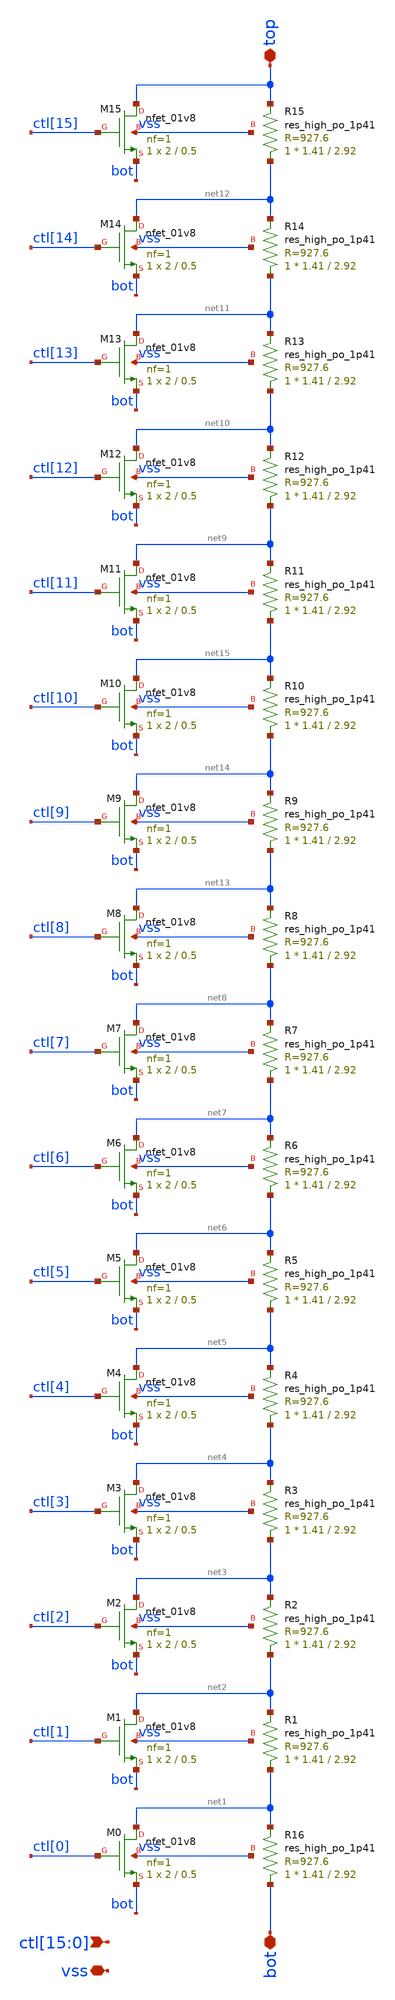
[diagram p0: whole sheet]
** sch_path: xschem/bandgap/bg_trim.sch
**.subckt bg_trim vss
*+ ctl[15],ctl[14],ctl[13],ctl[12],ctl[11],ctl[10],ctl[9],ctl[8],ctl[7],ctl[6],ctl[5],ctl[4],ctl[3],ctl[2],ctl[1],ctl[0] bot top
*.iopin vss
*.ipin
*+ ctl[15],ctl[14],ctl[13],ctl[12],ctl[11],ctl[10],ctl[9],ctl[8],ctl[7],ctl[6],ctl[5],ctl[4],ctl[3],ctl[2],ctl[1],ctl[0]
*.iopin bot
*.iopin top
XM0 net1 ctl[0] bot vss sky130_fd_pr__nfet_01v8 L=0.5 W=2 nf=1 ad='int((nf+1)/2) * W/nf * 0.29' as='int((nf+2)/2) * W/nf * 0.29'
+ pd='2*int((nf+1)/2) * (W/nf + 0.29)' ps='2*int((nf+2)/2) * (W/nf + 0.29)' nrd='0.29 / W' nrs='0.29 / W'
+ sa=0 sb=0 sd=0 mult=1 m=1
XM1 net2 ctl[1] bot vss sky130_fd_pr__nfet_01v8 L=0.5 W=2 nf=1 ad='int((nf+1)/2) * W/nf * 0.29' as='int((nf+2)/2) * W/nf * 0.29'
+ pd='2*int((nf+1)/2) * (W/nf + 0.29)' ps='2*int((nf+2)/2) * (W/nf + 0.29)' nrd='0.29 / W' nrs='0.29 / W'
+ sa=0 sb=0 sd=0 mult=1 m=1
XM2 net3 ctl[2] bot vss sky130_fd_pr__nfet_01v8 L=0.5 W=2 nf=1 ad='int((nf+1)/2) * W/nf * 0.29' as='int((nf+2)/2) * W/nf * 0.29'
+ pd='2*int((nf+1)/2) * (W/nf + 0.29)' ps='2*int((nf+2)/2) * (W/nf + 0.29)' nrd='0.29 / W' nrs='0.29 / W'
+ sa=0 sb=0 sd=0 mult=1 m=1
XM3 net4 ctl[3] bot vss sky130_fd_pr__nfet_01v8 L=0.5 W=2 nf=1 ad='int((nf+1)/2) * W/nf * 0.29' as='int((nf+2)/2) * W/nf * 0.29'
+ pd='2*int((nf+1)/2) * (W/nf + 0.29)' ps='2*int((nf+2)/2) * (W/nf + 0.29)' nrd='0.29 / W' nrs='0.29 / W'
+ sa=0 sb=0 sd=0 mult=1 m=1
XM4 net5 ctl[4] bot vss sky130_fd_pr__nfet_01v8 L=0.5 W=2 nf=1 ad='int((nf+1)/2) * W/nf * 0.29' as='int((nf+2)/2) * W/nf * 0.29'
+ pd='2*int((nf+1)/2) * (W/nf + 0.29)' ps='2*int((nf+2)/2) * (W/nf + 0.29)' nrd='0.29 / W' nrs='0.29 / W'
+ sa=0 sb=0 sd=0 mult=1 m=1
XM5 net6 ctl[5] bot vss sky130_fd_pr__nfet_01v8 L=0.5 W=2 nf=1 ad='int((nf+1)/2) * W/nf * 0.29' as='int((nf+2)/2) * W/nf * 0.29'
+ pd='2*int((nf+1)/2) * (W/nf + 0.29)' ps='2*int((nf+2)/2) * (W/nf + 0.29)' nrd='0.29 / W' nrs='0.29 / W'
+ sa=0 sb=0 sd=0 mult=1 m=1
XM6 net7 ctl[6] bot vss sky130_fd_pr__nfet_01v8 L=0.5 W=2 nf=1 ad='int((nf+1)/2) * W/nf * 0.29' as='int((nf+2)/2) * W/nf * 0.29'
+ pd='2*int((nf+1)/2) * (W/nf + 0.29)' ps='2*int((nf+2)/2) * (W/nf + 0.29)' nrd='0.29 / W' nrs='0.29 / W'
+ sa=0 sb=0 sd=0 mult=1 m=1
XM7 net8 ctl[7] bot vss sky130_fd_pr__nfet_01v8 L=0.5 W=2 nf=1 ad='int((nf+1)/2) * W/nf * 0.29' as='int((nf+2)/2) * W/nf * 0.29'
+ pd='2*int((nf+1)/2) * (W/nf + 0.29)' ps='2*int((nf+2)/2) * (W/nf + 0.29)' nrd='0.29 / W' nrs='0.29 / W'
+ sa=0 sb=0 sd=0 mult=1 m=1
XM12 net10 ctl[12] bot vss sky130_fd_pr__nfet_01v8 L=0.5 W=2 nf=1 ad='int((nf+1)/2) * W/nf * 0.29' as='int((nf+2)/2) * W/nf * 0.29'
+ pd='2*int((nf+1)/2) * (W/nf + 0.29)' ps='2*int((nf+2)/2) * (W/nf + 0.29)' nrd='0.29 / W' nrs='0.29 / W'
+ sa=0 sb=0 sd=0 mult=1 m=1
XM13 net11 ctl[13] bot vss sky130_fd_pr__nfet_01v8 L=0.5 W=2 nf=1 ad='int((nf+1)/2) * W/nf * 0.29' as='int((nf+2)/2) * W/nf * 0.29'
+ pd='2*int((nf+1)/2) * (W/nf + 0.29)' ps='2*int((nf+2)/2) * (W/nf + 0.29)' nrd='0.29 / W' nrs='0.29 / W'
+ sa=0 sb=0 sd=0 mult=1 m=1
XM14 net12 ctl[14] bot vss sky130_fd_pr__nfet_01v8 L=0.5 W=2 nf=1 ad='int((nf+1)/2) * W/nf * 0.29' as='int((nf+2)/2) * W/nf * 0.29'
+ pd='2*int((nf+1)/2) * (W/nf + 0.29)' ps='2*int((nf+2)/2) * (W/nf + 0.29)' nrd='0.29 / W' nrs='0.29 / W'
+ sa=0 sb=0 sd=0 mult=1 m=1
XM15 top ctl[15] bot vss sky130_fd_pr__nfet_01v8 L=0.5 W=2 nf=1 ad='int((nf+1)/2) * W/nf * 0.29' as='int((nf+2)/2) * W/nf * 0.29'
+ pd='2*int((nf+1)/2) * (W/nf + 0.29)' ps='2*int((nf+2)/2) * (W/nf + 0.29)' nrd='0.29 / W' nrs='0.29 / W'
+ sa=0 sb=0 sd=0 mult=1 m=1
XM8 net13 ctl[8] bot vss sky130_fd_pr__nfet_01v8 L=0.5 W=2 nf=1 ad='int((nf+1)/2) * W/nf * 0.29' as='int((nf+2)/2) * W/nf * 0.29'
+ pd='2*int((nf+1)/2) * (W/nf + 0.29)' ps='2*int((nf+2)/2) * (W/nf + 0.29)' nrd='0.29 / W' nrs='0.29 / W'
+ sa=0 sb=0 sd=0 mult=1 m=1
XM9 net14 ctl[9] bot vss sky130_fd_pr__nfet_01v8 L=0.5 W=2 nf=1 ad='int((nf+1)/2) * W/nf * 0.29' as='int((nf+2)/2) * W/nf * 0.29'
+ pd='2*int((nf+1)/2) * (W/nf + 0.29)' ps='2*int((nf+2)/2) * (W/nf + 0.29)' nrd='0.29 / W' nrs='0.29 / W'
+ sa=0 sb=0 sd=0 mult=1 m=1
XM10 net15 ctl[10] bot vss sky130_fd_pr__nfet_01v8 L=0.5 W=2 nf=1 ad='int((nf+1)/2) * W/nf * 0.29' as='int((nf+2)/2) * W/nf * 0.29'
+ pd='2*int((nf+1)/2) * (W/nf + 0.29)' ps='2*int((nf+2)/2) * (W/nf + 0.29)' nrd='0.29 / W' nrs='0.29 / W'
+ sa=0 sb=0 sd=0 mult=1 m=1
XM11 net9 ctl[11] bot vss sky130_fd_pr__nfet_01v8 L=0.5 W=2 nf=1 ad='int((nf+1)/2) * W/nf * 0.29' as='int((nf+2)/2) * W/nf * 0.29'
+ pd='2*int((nf+1)/2) * (W/nf + 0.29)' ps='2*int((nf+2)/2) * (W/nf + 0.29)' nrd='0.29 / W' nrs='0.29 / W'
+ sa=0 sb=0 sd=0 mult=1 m=1
XR15 net12 top vss sky130_fd_pr__res_high_po_1p41 L=2.92 mult=1 m=1
XR1 net1 net2 vss sky130_fd_pr__res_high_po_1p41 L=2.92 mult=1 m=1
XR16 bot net1 vss sky130_fd_pr__res_high_po_1p41 L=2.92 mult=1 m=1
XR2 net2 net3 vss sky130_fd_pr__res_high_po_1p41 L=2.92 mult=1 m=1
XR3 net3 net4 vss sky130_fd_pr__res_high_po_1p41 L=2.92 mult=1 m=1
XR4 net4 net5 vss sky130_fd_pr__res_high_po_1p41 L=2.92 mult=1 m=1
XR5 net5 net6 vss sky130_fd_pr__res_high_po_1p41 L=2.92 mult=1 m=1
XR6 net6 net7 vss sky130_fd_pr__res_high_po_1p41 L=2.92 mult=1 m=1
XR7 net7 net8 vss sky130_fd_pr__res_high_po_1p41 L=2.92 mult=1 m=1
XR8 net8 net13 vss sky130_fd_pr__res_high_po_1p41 L=2.92 mult=1 m=1
XR9 net13 net14 vss sky130_fd_pr__res_high_po_1p41 L=2.92 mult=1 m=1
XR10 net14 net15 vss sky130_fd_pr__res_high_po_1p41 L=2.92 mult=1 m=1
XR11 net15 net9 vss sky130_fd_pr__res_high_po_1p41 L=2.92 mult=1 m=1
XR12 net9 net10 vss sky130_fd_pr__res_high_po_1p41 L=2.92 mult=1 m=1
XR13 net10 net11 vss sky130_fd_pr__res_high_po_1p41 L=2.92 mult=1 m=1
XR14 net11 net12 vss sky130_fd_pr__res_high_po_1p41 L=2.92 mult=1 m=1
**.ends
.end
